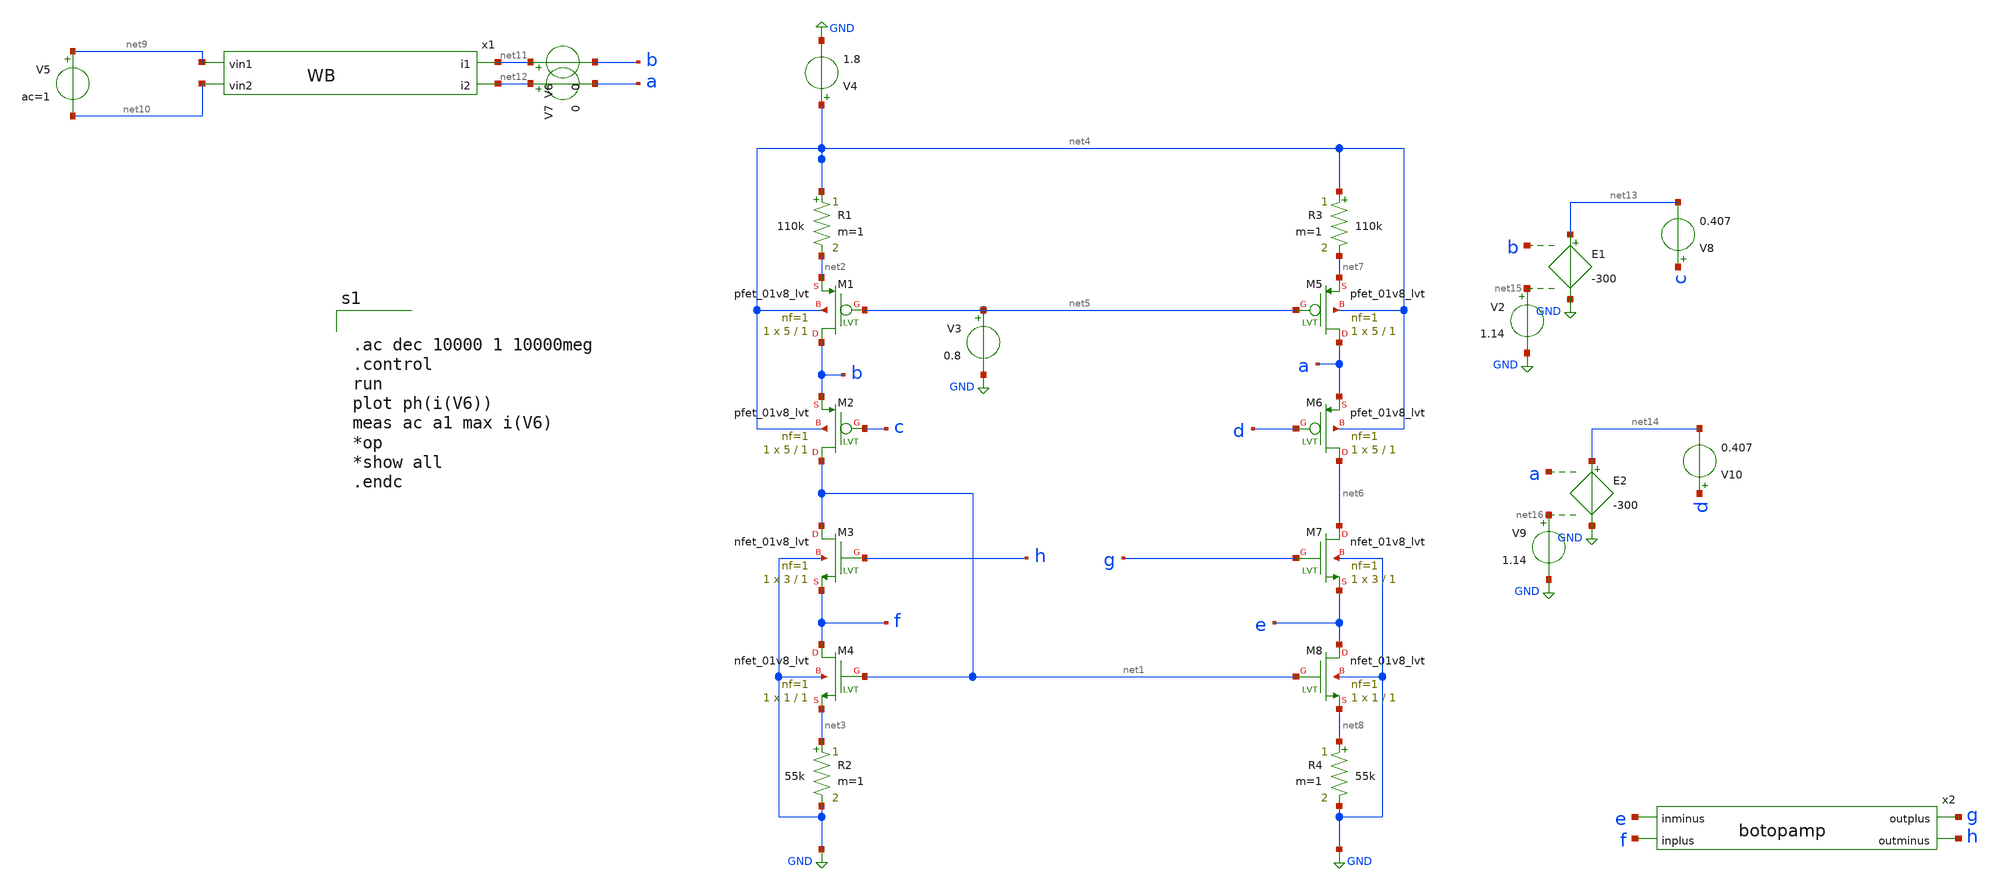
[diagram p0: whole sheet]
** sch_path: CB.sch
**.subckt CB
XM1 b net5 net2 net4 sky130_fd_pr__pfet_01v8_lvt L=1 W=5 nf=1 ad='int((nf+1)/2) * W/nf * 0.29' as='int((nf+2)/2) * W/nf * 0.29'
+ pd='2*int((nf+1)/2) * (W/nf + 0.29)' ps='2*int((nf+2)/2) * (W/nf + 0.29)' nrd='0.29 / W' nrs='0.29 / W'
+ sa=0 sb=0 sd=0 mult=1 m=1
XM2 net1 c b net4 sky130_fd_pr__pfet_01v8_lvt L=1 W=5 nf=1 ad='int((nf+1)/2) * W/nf * 0.29' as='int((nf+2)/2) * W/nf * 0.29'
+ pd='2*int((nf+1)/2) * (W/nf + 0.29)' ps='2*int((nf+2)/2) * (W/nf + 0.29)' nrd='0.29 / W' nrs='0.29 / W'
+ sa=0 sb=0 sd=0 mult=1 m=1
XM3 net1 h f GND sky130_fd_pr__nfet_01v8_lvt L=1 W=3 nf=1 ad='int((nf+1)/2) * W/nf * 0.29' as='int((nf+2)/2) * W/nf * 0.29'
+ pd='2*int((nf+1)/2) * (W/nf + 0.29)' ps='2*int((nf+2)/2) * (W/nf + 0.29)' nrd='0.29 / W' nrs='0.29 / W'
+ sa=0 sb=0 sd=0 mult=1 m=1
XM4 f net1 net3 GND sky130_fd_pr__nfet_01v8_lvt L=1 W=1 nf=1 ad='int((nf+1)/2) * W/nf * 0.29' as='int((nf+2)/2) * W/nf * 0.29'
+ pd='2*int((nf+1)/2) * (W/nf + 0.29)' ps='2*int((nf+2)/2) * (W/nf + 0.29)' nrd='0.29 / W' nrs='0.29 / W'
+ sa=0 sb=0 sd=0 mult=1 m=1
R1 net4 net2 110k m=1
R2 net3 GND 55k m=1
V3 net5 GND 0.8
V4 net4 GND 1.8
XM5 a net5 net7 net4 sky130_fd_pr__pfet_01v8_lvt L=1 W=5 nf=1 ad='int((nf+1)/2) * W/nf * 0.29' as='int((nf+2)/2) * W/nf * 0.29'
+ pd='2*int((nf+1)/2) * (W/nf + 0.29)' ps='2*int((nf+2)/2) * (W/nf + 0.29)' nrd='0.29 / W' nrs='0.29 / W'
+ sa=0 sb=0 sd=0 mult=1 m=1
XM6 net6 d a net4 sky130_fd_pr__pfet_01v8_lvt L=1 W=5 nf=1 ad='int((nf+1)/2) * W/nf * 0.29' as='int((nf+2)/2) * W/nf * 0.29'
+ pd='2*int((nf+1)/2) * (W/nf + 0.29)' ps='2*int((nf+2)/2) * (W/nf + 0.29)' nrd='0.29 / W' nrs='0.29 / W'
+ sa=0 sb=0 sd=0 mult=1 m=1
XM7 net6 g e GND sky130_fd_pr__nfet_01v8_lvt L=1 W=3 nf=1 ad='int((nf+1)/2) * W/nf * 0.29' as='int((nf+2)/2) * W/nf * 0.29'
+ pd='2*int((nf+1)/2) * (W/nf + 0.29)' ps='2*int((nf+2)/2) * (W/nf + 0.29)' nrd='0.29 / W' nrs='0.29 / W'
+ sa=0 sb=0 sd=0 mult=1 m=1
XM8 e net1 net8 GND sky130_fd_pr__nfet_01v8_lvt L=1 W=1 nf=1 ad='int((nf+1)/2) * W/nf * 0.29' as='int((nf+2)/2) * W/nf * 0.29'
+ pd='2*int((nf+1)/2) * (W/nf + 0.29)' ps='2*int((nf+2)/2) * (W/nf + 0.29)' nrd='0.29 / W' nrs='0.29 / W'
+ sa=0 sb=0 sd=0 mult=1 m=1
R3 net4 net7 110k m=1
R4 net8 GND 55k m=1
x1 net9 net11 net12 net10 WB
V5 net9 net10 ac=1
V6 net11 b 0
V7 net12 a 0
E1 net13 GND b net15 -300
V2 net15 GND 1.14
V8 c net13 0.407
E2 net14 GND a net16 -300
V9 net16 GND 1.14
V10 d net14 0.407
x2 g h e f botopamp
**** begin user architecture code

.lib ~/open_pdks/sky130/sky130A/libs.tech/ngspice/sky130.lib.spice tt
*.param mc_mm_switch=0
*.param mc_pr_switch=0

*.include ~/open_pdks/sky130/sky130A/libs.tech/ngspice/corners/tt/nonfet.spice


*model
*.include ~/open_pdks/sky130/sky130A/libs.tech/ngspice/all.spice

*mosfet
*.include ~/open_pdks/sky130/sky130A/libs.ref/sky130_fd_pr/spice/sky130_fd_pr__pfet_01v8_lvt__tt.corner.spice
*.inclued ~/open_pdks/sky130/sky130A/libs.ref/sky130_fd_pr/spice/sky130_fd_pr__nfet_01v8_lvt__tt.corner.spice

*mismatch parameters
*.include ~/open_pdks/sky130/sky130A/libs.ref/sky130_fd_pr/spice/sky130_fd_pr__pfet_01v8_lvt__mismatch.corner.spice
*.include ~/open_pdks/sky130/sky130A/libs.ref/sky130_fd_pr/spice/sky130_fd_pr__nfet_01v8_lvt__mismatch.corner.spice



.ac dec 10000 1 10000meg
.control
run
plot ph(i(V6))
meas ac a1 max i(V6)
*op
*show all
.endc

**** end user architecture code
**.ends
.GLOBAL GND
.end
